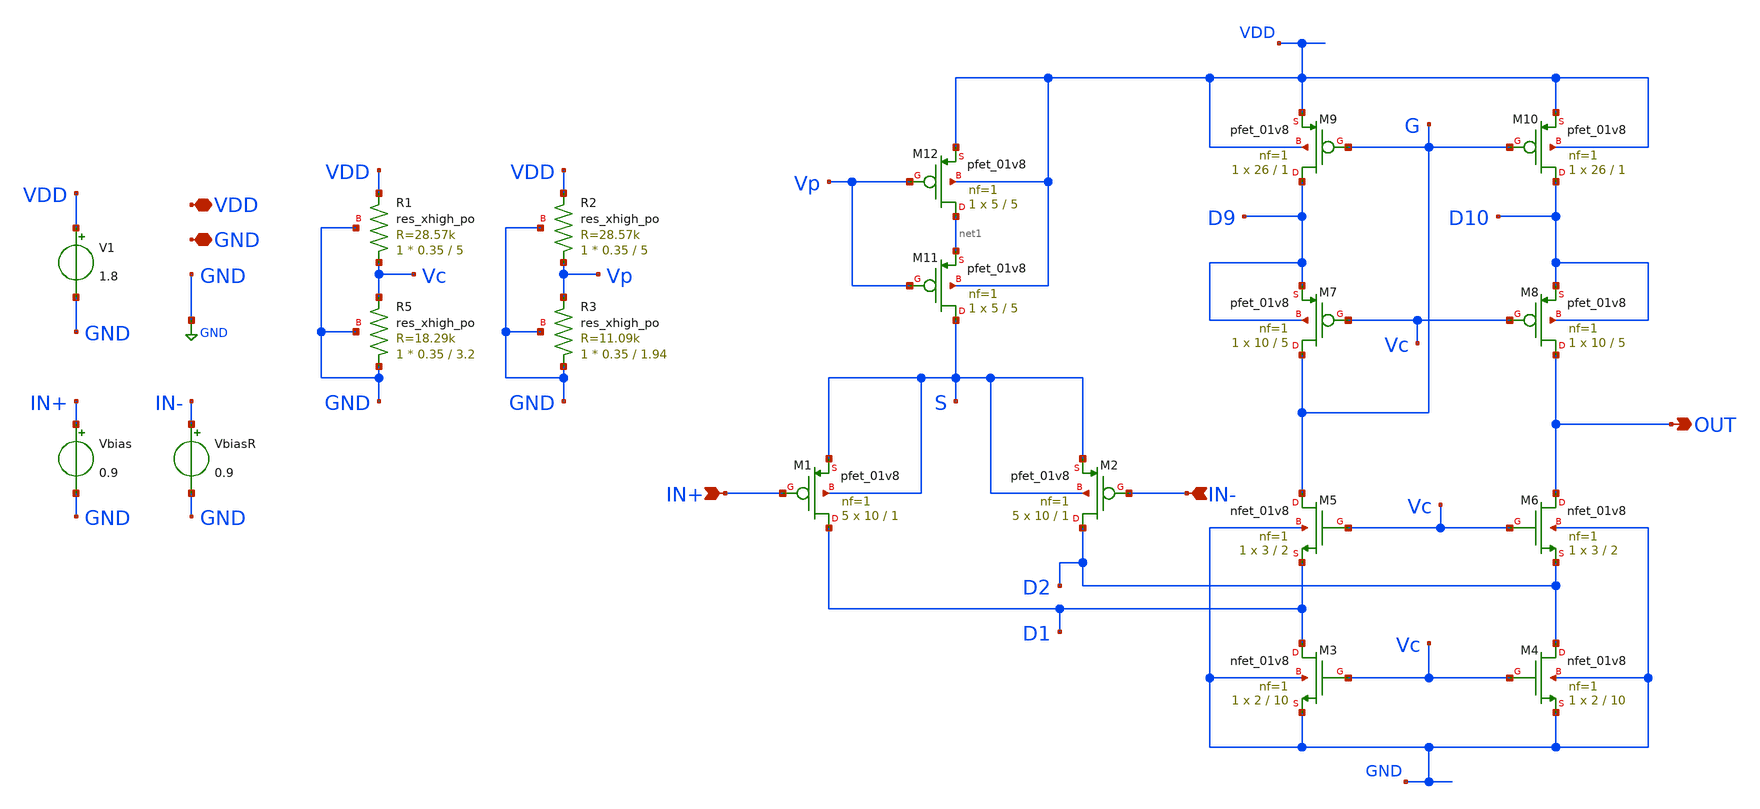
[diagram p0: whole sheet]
** sch_path: xschem/OTA_FoldedCascode.sch
**.subckt OTA_FoldedCascode VDD GND IN+ IN- OUT
*.iopin VDD
*.iopin GND
*.ipin IN+
*.ipin IN-
*.opin OUT
V1 VDD GND 1.8
Vbias IN+ GND 0.9
VbiasR IN- GND 0.9
XM1 D1 IN+ S S sky130_fd_pr__pfet_01v8 L=1 W=10 nf=1 ad='int((nf+1)/2) * W/nf * 0.29' as='int((nf+2)/2) * W/nf * 0.29'
+ pd='2*int((nf+1)/2) * (W/nf + 0.29)' ps='2*int((nf+2)/2) * (W/nf + 0.29)' nrd='0.29 / W' nrs='0.29 / W'
+ sa=0 sb=0 sd=0 mult=5 m=5
XM2 D2 IN- S S sky130_fd_pr__pfet_01v8 L=1 W=10 nf=1 ad='int((nf+1)/2) * W/nf * 0.29' as='int((nf+2)/2) * W/nf * 0.29'
+ pd='2*int((nf+1)/2) * (W/nf + 0.29)' ps='2*int((nf+2)/2) * (W/nf + 0.29)' nrd='0.29 / W' nrs='0.29 / W'
+ sa=0 sb=0 sd=0 mult=5 m=5
XM3 D1 Vc GND GND sky130_fd_pr__nfet_01v8 L=10 W=2 nf=1 ad='int((nf+1)/2) * W/nf * 0.29' as='int((nf+2)/2) * W/nf * 0.29'
+ pd='2*int((nf+1)/2) * (W/nf + 0.29)' ps='2*int((nf+2)/2) * (W/nf + 0.29)' nrd='0.29 / W' nrs='0.29 / W'
+ sa=0 sb=0 sd=0 mult=1 m=1
XM4 D2 Vc GND GND sky130_fd_pr__nfet_01v8 L=10 W=2 nf=1 ad='int((nf+1)/2) * W/nf * 0.29' as='int((nf+2)/2) * W/nf * 0.29'
+ pd='2*int((nf+1)/2) * (W/nf + 0.29)' ps='2*int((nf+2)/2) * (W/nf + 0.29)' nrd='0.29 / W' nrs='0.29 / W'
+ sa=0 sb=0 sd=0 mult=1 m=1
XM5 G Vc D1 GND sky130_fd_pr__nfet_01v8 L=2 W=3 nf=1 ad='int((nf+1)/2) * W/nf * 0.29' as='int((nf+2)/2) * W/nf * 0.29'
+ pd='2*int((nf+1)/2) * (W/nf + 0.29)' ps='2*int((nf+2)/2) * (W/nf + 0.29)' nrd='0.29 / W' nrs='0.29 / W'
+ sa=0 sb=0 sd=0 mult=1 m=1
XM6 OUT Vc D2 GND sky130_fd_pr__nfet_01v8 L=2 W=3 nf=1 ad='int((nf+1)/2) * W/nf * 0.29' as='int((nf+2)/2) * W/nf * 0.29'
+ pd='2*int((nf+1)/2) * (W/nf + 0.29)' ps='2*int((nf+2)/2) * (W/nf + 0.29)' nrd='0.29 / W' nrs='0.29 / W'
+ sa=0 sb=0 sd=0 mult=1 m=1
XM7 G Vc D9 D9 sky130_fd_pr__pfet_01v8 L=5 W=10 nf=1 ad='int((nf+1)/2) * W/nf * 0.29' as='int((nf+2)/2) * W/nf * 0.29'
+ pd='2*int((nf+1)/2) * (W/nf + 0.29)' ps='2*int((nf+2)/2) * (W/nf + 0.29)' nrd='0.29 / W' nrs='0.29 / W'
+ sa=0 sb=0 sd=0 mult=1 m=1
XM8 OUT Vc D10 D10 sky130_fd_pr__pfet_01v8 L=5 W=10 nf=1 ad='int((nf+1)/2) * W/nf * 0.29' as='int((nf+2)/2) * W/nf * 0.29'
+ pd='2*int((nf+1)/2) * (W/nf + 0.29)' ps='2*int((nf+2)/2) * (W/nf + 0.29)' nrd='0.29 / W' nrs='0.29 / W'
+ sa=0 sb=0 sd=0 mult=1 m=1
XM9 D9 G VDD VDD sky130_fd_pr__pfet_01v8 L=1 W=26 nf=1 ad='int((nf+1)/2) * W/nf * 0.29' as='int((nf+2)/2) * W/nf * 0.29'
+ pd='2*int((nf+1)/2) * (W/nf + 0.29)' ps='2*int((nf+2)/2) * (W/nf + 0.29)' nrd='0.29 / W' nrs='0.29 / W'
+ sa=0 sb=0 sd=0 mult=1 m=1
XM10 D10 G VDD VDD sky130_fd_pr__pfet_01v8 L=1 W=26 nf=1 ad='int((nf+1)/2) * W/nf * 0.29' as='int((nf+2)/2) * W/nf * 0.29'
+ pd='2*int((nf+1)/2) * (W/nf + 0.29)' ps='2*int((nf+2)/2) * (W/nf + 0.29)' nrd='0.29 / W' nrs='0.29 / W'
+ sa=0 sb=0 sd=0 mult=1 m=1
XM11 S Vp net1 VDD sky130_fd_pr__pfet_01v8 L=5 W=5 nf=1 ad='int((nf+1)/2) * W/nf * 0.29' as='int((nf+2)/2) * W/nf * 0.29'
+ pd='2*int((nf+1)/2) * (W/nf + 0.29)' ps='2*int((nf+2)/2) * (W/nf + 0.29)' nrd='0.29 / W' nrs='0.29 / W'
+ sa=0 sb=0 sd=0 mult=1 m=1
XM12 net1 Vp VDD VDD sky130_fd_pr__pfet_01v8 L=5 W=5 nf=1 ad='int((nf+1)/2) * W/nf * 0.29' as='int((nf+2)/2) * W/nf * 0.29'
+ pd='2*int((nf+1)/2) * (W/nf + 0.29)' ps='2*int((nf+2)/2) * (W/nf + 0.29)' nrd='0.29 / W' nrs='0.29 / W'
+ sa=0 sb=0 sd=0 mult=1 m=1
XR5 GND Vc GND sky130_fd_pr__res_xhigh_po W=0.35 L=3.2 mult=1 m=1
XR1 Vc VDD GND sky130_fd_pr__res_xhigh_po W=0.35 L=5 mult=1 m=1
XR2 Vp VDD GND sky130_fd_pr__res_xhigh_po W=0.35 L=5 mult=1 m=1
XR3 GND Vp GND sky130_fd_pr__res_xhigh_po W=0.35 L=1.94 mult=1 m=1
**** begin user architecture code



* ngspice commands

.options savecurrents

.control
save all
save @m.xm1.msky130_fd_pr__pfet_01v8[gm]
save @m.xm2.msky130_fd_pr__pfet_01v8[gm]
save @m.xm3.msky130_fd_pr__nfet_01v8[gm]
save @m.xm4.msky130_fd_pr__nfet_01v8[gm]
save @m.xm5.msky130_fd_pr__nfet_01v8[gm]
save @m.xm6.msky130_fd_pr__nfet_01v8[gm]
save @m.xm7.msky130_fd_pr__pfet_01v8[gm]
save @m.xm8.msky130_fd_pr__pfet_01v8[gm]
save @m.xm9.msky130_fd_pr__pfet_01v8[gm]
save @m.xm10.msky130_fd_pr__pfet_01v8[gm]

   op
   remzerovec
   write OTA_FoldedCascode.raw
   set appendwrite
   *dc Vbias 0.899 0.901 0.00001

   dc Vbias 0.8 1 0.001
   *remzerovec
   plot v(out),v(in+)
   plot deriv(v(out))

   write OTA_FoldedCascode.raw
.measure gain max(deriv(v(out)))
.endc
.end



.lib $::SKYWATER_MODELS/sky130.lib.spice tt
**** end user architecture code
**.ends
.GLOBAL GND
.end
